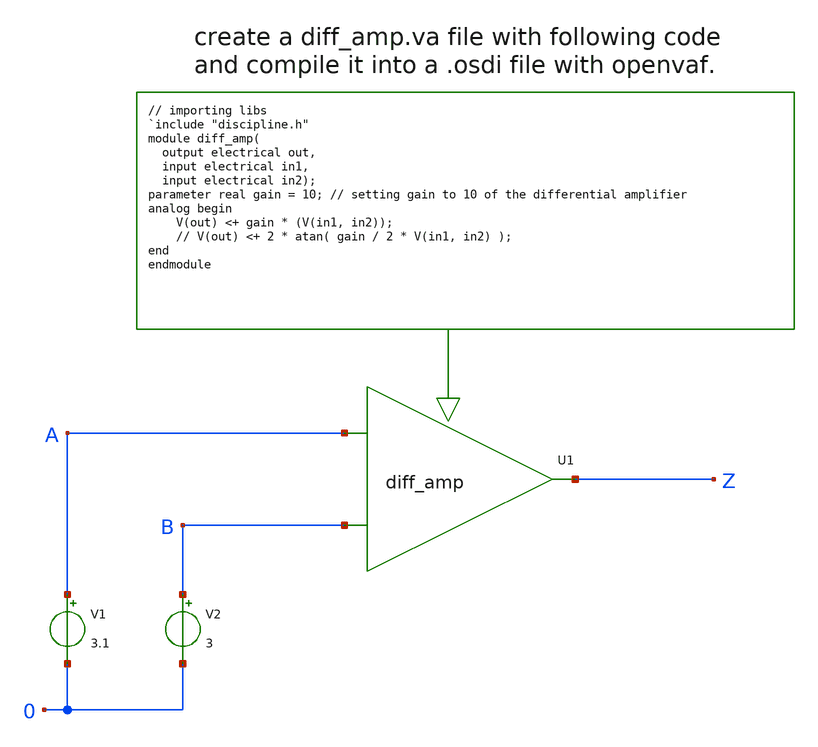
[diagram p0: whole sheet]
** sch_path: sky130A/xschem_libs/sky130_tests_ase/tb_diff_amp/schematic/tb_diff_amp.sch
**.subckt tb_diff_amp
XU1 Z A B diff_amp_cell
V1 A 0 3.1
V2 B 0 3
**.ends
**** begin user architecture code

.subckt diff_amp_cell OUT IN1 IN2
N1 out in1 in2 diff_amp_model
.ends diff_amp_cell

.model diff_amp_model diff_amp

.control
* following line specifies the location for the .osdi file so ngspice can use it.
pre_osdi $USER_CONF_DIR/xschem_library/diff_amp.osdi
.endc

**** end user architecture code
.end
